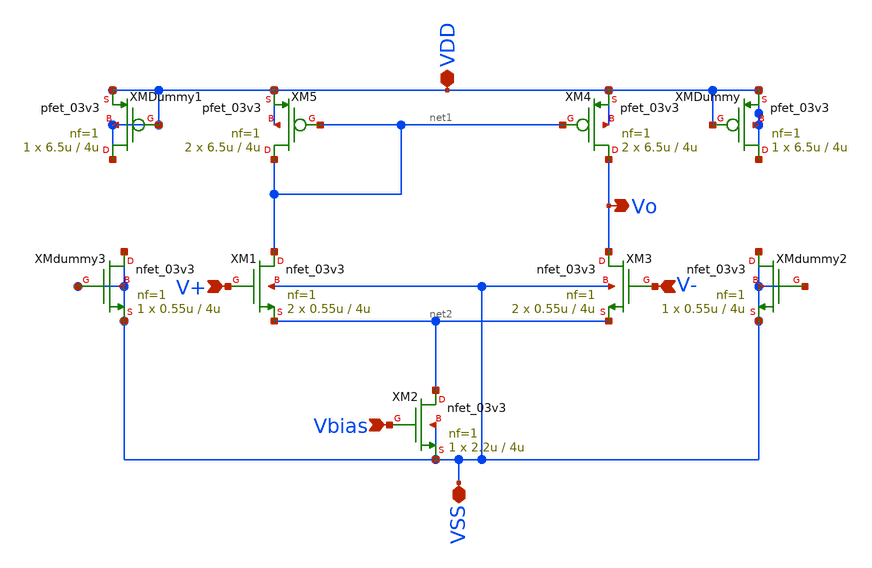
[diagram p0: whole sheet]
** sch_path: analog/B04_diff_amp.sch
**.subckt B04_diff_amp VDD VSS V+ V- Vo Vbias
*.iopin VDD
*.iopin VSS
*.ipin V+
*.ipin V-
*.opin Vo
*.ipin Vbias
XM1 net1 V+ net2 VSS nfet_03v3 L=4u W=0.55u nf=1 ad='int((nf+1)/2) * W/nf * 0.18u' as='int((nf+2)/2) * W/nf * 0.18u'
+ pd='2*int((nf+1)/2) * (W/nf + 0.18u)' ps='2*int((nf+2)/2) * (W/nf + 0.18u)' nrd='0.18u / W' nrs='0.18u / W'
+ sa=0 sb=0 sd=0 m=2
XM2 net2 Vbias VSS VSS nfet_03v3 L=4u W=2.2u nf=1 ad='int((nf+1)/2) * W/nf * 0.18u' as='int((nf+2)/2) * W/nf * 0.18u'
+ pd='2*int((nf+1)/2) * (W/nf + 0.18u)' ps='2*int((nf+2)/2) * (W/nf + 0.18u)' nrd='0.18u / W' nrs='0.18u / W'
+ sa=0 sb=0 sd=0 m=1
XM3 Vo V- net2 VSS nfet_03v3 L=4u W=0.55u nf=1 ad='int((nf+1)/2) * W/nf * 0.18u' as='int((nf+2)/2) * W/nf * 0.18u'
+ pd='2*int((nf+1)/2) * (W/nf + 0.18u)' ps='2*int((nf+2)/2) * (W/nf + 0.18u)' nrd='0.18u / W' nrs='0.18u / W'
+ sa=0 sb=0 sd=0 m=2
XM4 Vo net1 VDD VDD pfet_03v3 L=4u W=6.5u nf=1 ad='int((nf+1)/2) * W/nf * 0.18u' as='int((nf+2)/2) * W/nf * 0.18u'
+ pd='2*int((nf+1)/2) * (W/nf + 0.18u)' ps='2*int((nf+2)/2) * (W/nf + 0.18u)' nrd='0.18u / W' nrs='0.18u / W'
+ sa=0 sb=0 sd=0 m=2
XM5 net1 net1 VDD VDD pfet_03v3 L=4u W=6.5u nf=1 ad='int((nf+1)/2) * W/nf * 0.18u' as='int((nf+2)/2) * W/nf * 0.18u'
+ pd='2*int((nf+1)/2) * (W/nf + 0.18u)' ps='2*int((nf+2)/2) * (W/nf + 0.18u)' nrd='0.18u / W' nrs='0.18u / W'
+ sa=0 sb=0 sd=0 m=2
XMDummy VDD VDD VDD VDD pfet_03v3 L=4u W=6.5u nf=1 ad='int((nf+1)/2) * W/nf * 0.18u' as='int((nf+2)/2) * W/nf * 0.18u'
+ pd='2*int((nf+1)/2) * (W/nf + 0.18u)' ps='2*int((nf+2)/2) * (W/nf + 0.18u)' nrd='0.18u / W' nrs='0.18u / W'
+ sa=0 sb=0 sd=0 m=1
XMDummy1 VDD VDD VDD VDD pfet_03v3 L=4u W=6.5u nf=1 ad='int((nf+1)/2) * W/nf * 0.18u' as='int((nf+2)/2) * W/nf * 0.18u'
+ pd='2*int((nf+1)/2) * (W/nf + 0.18u)' ps='2*int((nf+2)/2) * (W/nf + 0.18u)' nrd='0.18u / W' nrs='0.18u / W'
+ sa=0 sb=0 sd=0 m=1
XMdummy2 VSS VSS VSS VSS nfet_03v3 L=4u W=0.55u nf=1 ad='int((nf+1)/2) * W/nf * 0.18u' as='int((nf+2)/2) * W/nf * 0.18u'
+ pd='2*int((nf+1)/2) * (W/nf + 0.18u)' ps='2*int((nf+2)/2) * (W/nf + 0.18u)' nrd='0.18u / W' nrs='0.18u / W'
+ sa=0 sb=0 sd=0 m=1
XMdummy3 VSS VSS VSS VSS nfet_03v3 L=4u W=0.55u nf=1 ad='int((nf+1)/2) * W/nf * 0.18u' as='int((nf+2)/2) * W/nf * 0.18u'
+ pd='2*int((nf+1)/2) * (W/nf + 0.18u)' ps='2*int((nf+2)/2) * (W/nf + 0.18u)' nrd='0.18u / W' nrs='0.18u / W'
+ sa=0 sb=0 sd=0 m=1
**.ends
.end
